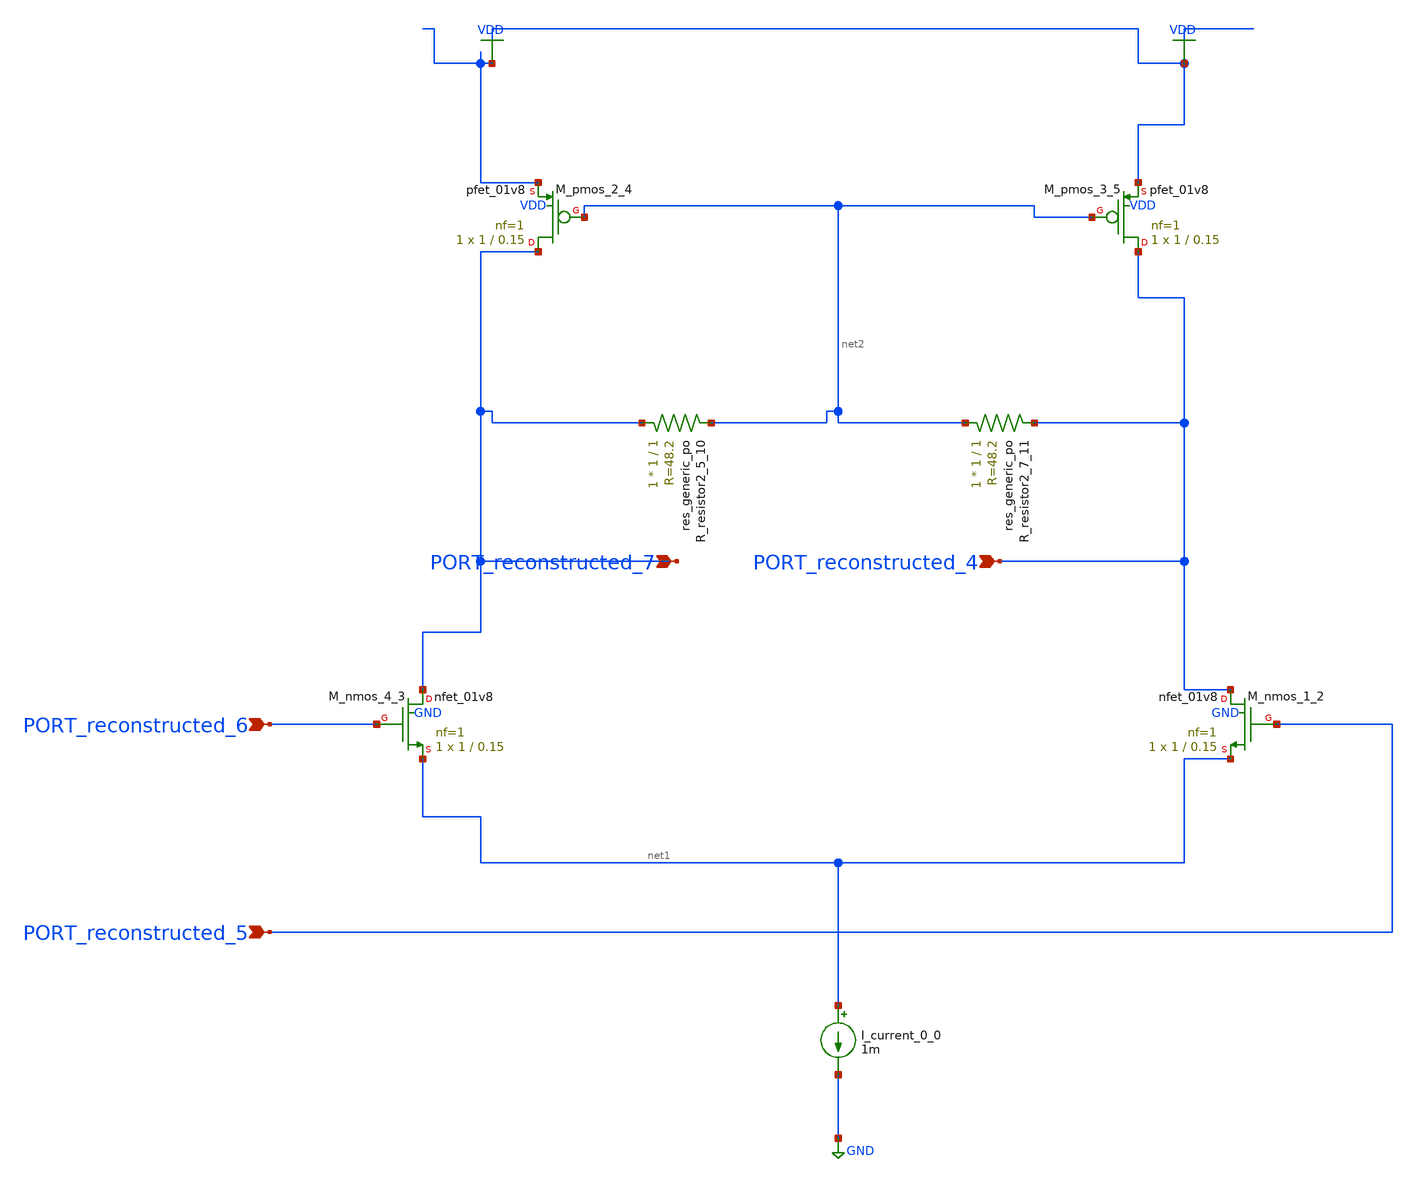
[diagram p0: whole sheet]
** sch_path: schematics/AMSNet/674.sch
**.subckt 674 PORT_reconstructed_5 PORT_reconstructed_4 PORT_reconstructed_6 PORT_reconstructed_7
*.ipin PORT_reconstructed_5
*.ipin PORT_reconstructed_4
*.ipin PORT_reconstructed_6
*.ipin PORT_reconstructed_7
I_current_0_0 net1 GND 1m
XM_nmos_1_2 PORT_reconstructed_4 PORT_reconstructed_5 net1 GND sky130_fd_pr__nfet_01v8 L=0.15 W=1 nf=1
+ ad='int((1 + 1)/2) * 1 / 1 * 0.29' as='int((1 + 2)/2) * 1 / 1 * 0.29' pd='2*int((1 + 1)/2) * (1 / 1 + 0.29)'
+ ps='2*int((1 + 2)/2) * (1 / 1 + 0.29)' nrd='0.29 / 1 ' nrs='0.29 / 1 ' sa=0 sb=0 sd=0 mult=1 m=1
XM_nmos_4_3 PORT_reconstructed_7 PORT_reconstructed_6 net1 GND sky130_fd_pr__nfet_01v8 L=0.15 W=1 nf=1
+ ad='int((1 + 1)/2) * 1 / 1 * 0.29' as='int((1 + 2)/2) * 1 / 1 * 0.29' pd='2*int((1 + 1)/2) * (1 / 1 + 0.29)'
+ ps='2*int((1 + 2)/2) * (1 / 1 + 0.29)' nrd='0.29 / 1 ' nrs='0.29 / 1 ' sa=0 sb=0 sd=0 mult=1 m=1
XM_pmos_2_4 PORT_reconstructed_7 net2 VDD VDD sky130_fd_pr__pfet_01v8 L=0.15 W=1 nf=1 ad='int((1 + 1)/2) * 1 / 1 * 0.29'
+ as='int((1 + 2)/2) * 1 / 1 * 0.29' pd='2*int((1 + 1)/2) * (1 / 1 + 0.29)' ps='2*int((1 + 2)/2) * (1 / 1 + 0.29)'
+ nrd='0.29 / 1 ' nrs='0.29 / 1 ' sa=0 sb=0 sd=0 mult=1 m=1
XM_pmos_3_5 PORT_reconstructed_4 net2 VDD VDD sky130_fd_pr__pfet_01v8 L=0.15 W=1 nf=1 ad='int((1 + 1)/2) * 1 / 1 * 0.29'
+ as='int((1 + 2)/2) * 1 / 1 * 0.29' pd='2*int((1 + 1)/2) * (1 / 1 + 0.29)' ps='2*int((1 + 2)/2) * (1 / 1 + 0.29)'
+ nrd='0.29 / 1 ' nrs='0.29 / 1 ' sa=0 sb=0 sd=0 mult=1 m=1
XR_resistor2_5_10 PORT_reconstructed_7 net2 sky130_fd_pr__res_generic_po W=1 L=1 m=1
XR_resistor2_7_11 net2 PORT_reconstructed_4 sky130_fd_pr__res_generic_po W=1 L=1 m=1
**.ends
.GLOBAL GND
.GLOBAL VDD
.end
